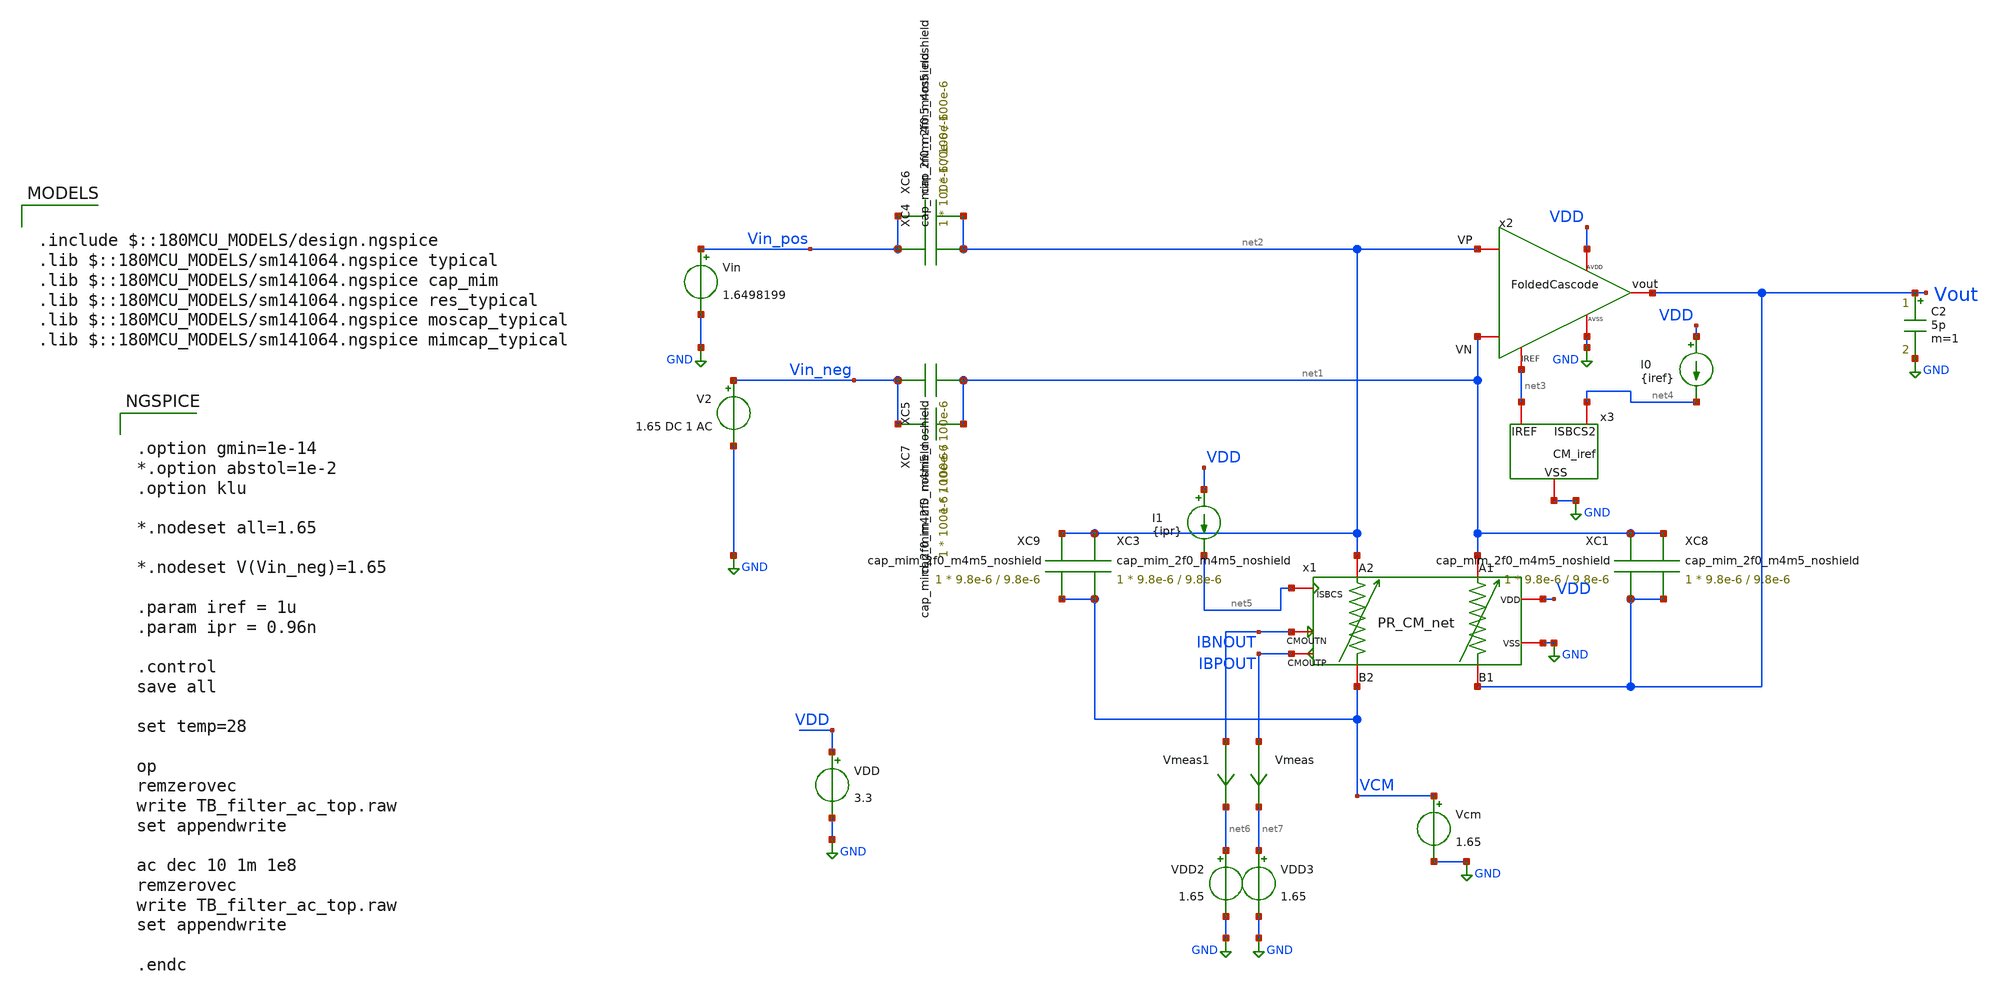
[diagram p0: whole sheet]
** sch_path: TIA_Filter/TB_filter_ac_top.sch
**.subckt TB_filter_ac_top
C2 Vout GND 5p m=1
V2 Vin_neg GND 1.65 DC 1 AC
x1 net5 net1 net2 VCM Vout IBNOUT IBPOUT VDD GND PR_CM_net
XC1 net1 Vout cap_mim_2f0_m4m5_noshield c_width=9.8e-6 c_length=9.8e-6 m=1
x2 net2 net1 Vout net3 VDD GND FoldedCascode
XC3 net2 VCM cap_mim_2f0_m4m5_noshield c_width=9.8e-6 c_length=9.8e-6 m=1
XC4 Vin_pos net2 cap_mim_2f0_m4m5_noshield c_width=100e-6 c_length=100e-6 m=1
XC5 Vin_neg net1 cap_mim_2f0_m4m5_noshield c_width=100e-6 c_length=100e-6 m=1
x3 net4 net3 GND CM_iref
I0 VDD net4 {iref}
I1 VDD net5 {ipr}
Vmeas IBPOUT net7 0
.save i(vmeas)
Vmeas1 IBNOUT net6 0
.save i(vmeas1)
Vcm VCM GND 1.65
VDD2 net6 GND 1.65
VDD3 net7 GND 1.65
VDD VDD GND 3.3
XC6 Vin_pos net2 cap_mim_2f0_m4m5_noshield c_width=100e-6 c_length=100e-6 m=1
XC7 Vin_neg net1 cap_mim_2f0_m4m5_noshield c_width=100e-6 c_length=100e-6 m=1
XC8 net1 Vout cap_mim_2f0_m4m5_noshield c_width=9.8e-6 c_length=9.8e-6 m=1
XC9 net2 VCM cap_mim_2f0_m4m5_noshield c_width=9.8e-6 c_length=9.8e-6 m=1
Vin Vin_pos GND 1.6498199
**** begin user architecture code

.include $::180MCU_MODELS/design.ngspice
.lib $::180MCU_MODELS/sm141064.ngspice typical
.lib $::180MCU_MODELS/sm141064.ngspice cap_mim
.lib $::180MCU_MODELS/sm141064.ngspice res_typical
.lib $::180MCU_MODELS/sm141064.ngspice moscap_typical
.lib $::180MCU_MODELS/sm141064.ngspice mimcap_typical



.option gmin=1e-14
*.option abstol=1e-2
.option klu

*.nodeset all=1.65

*.nodeset V(Vin_neg)=1.65

.param iref = 1u
.param ipr = 0.96n

.control
save all

set temp=28

op
remzerovec
write TB_filter_ac_top.raw
set appendwrite

ac dec 10 1m 1e8
remzerovec
write TB_filter_ac_top.raw
set appendwrite

.endc


**** end user architecture code
**.ends
.GLOBAL GND
.end
